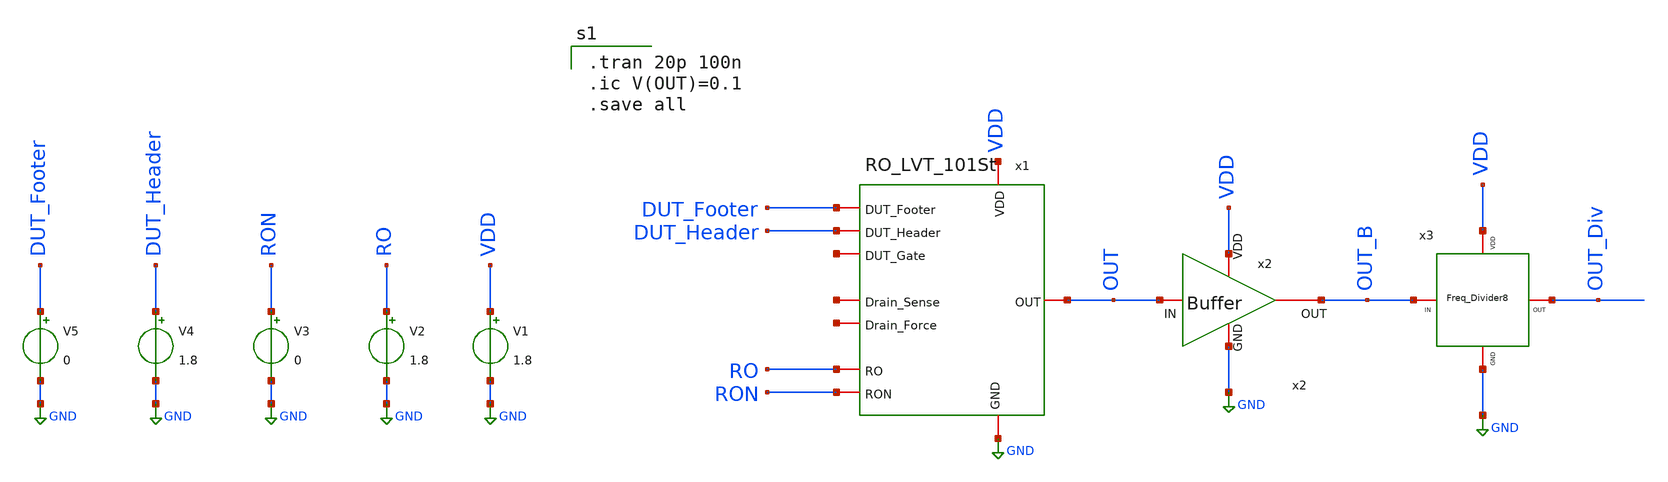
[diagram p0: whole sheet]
** sch_path: TB/101St_TB.sch
**.subckt 101St_TB
V1 VDD GND 1.8
V2 RO GND 1.8
V3 RON GND 0
V4 DUT_Header GND 1.8
V5 DUT_Footer GND 0
x1 VDD GND DUT_Footer DUT_Header net1 net2 RO RON net3 OUT RO_LVT_101St
x2 VDD OUT OUT_B GND Buffer
x3 OUT_B OUT_Div VDD GND Freq_Divider8
**** begin user architecture code
 .lib $::SKYWATER_MODELS/sky130.lib.spice tt
.include $::SKYWATER_STDCELLS/sky130_fd_sc_hd.spice


.tran 20p 100n
.ic V(OUT)=0.1
.save all

**** end user architecture code
**.ends
.GLOBAL GND
.GLOBAL VDD
.GLOBAL RO
.GLOBAL RON
.GLOBAL DUT_Header
.GLOBAL DUT_Footer
.end
